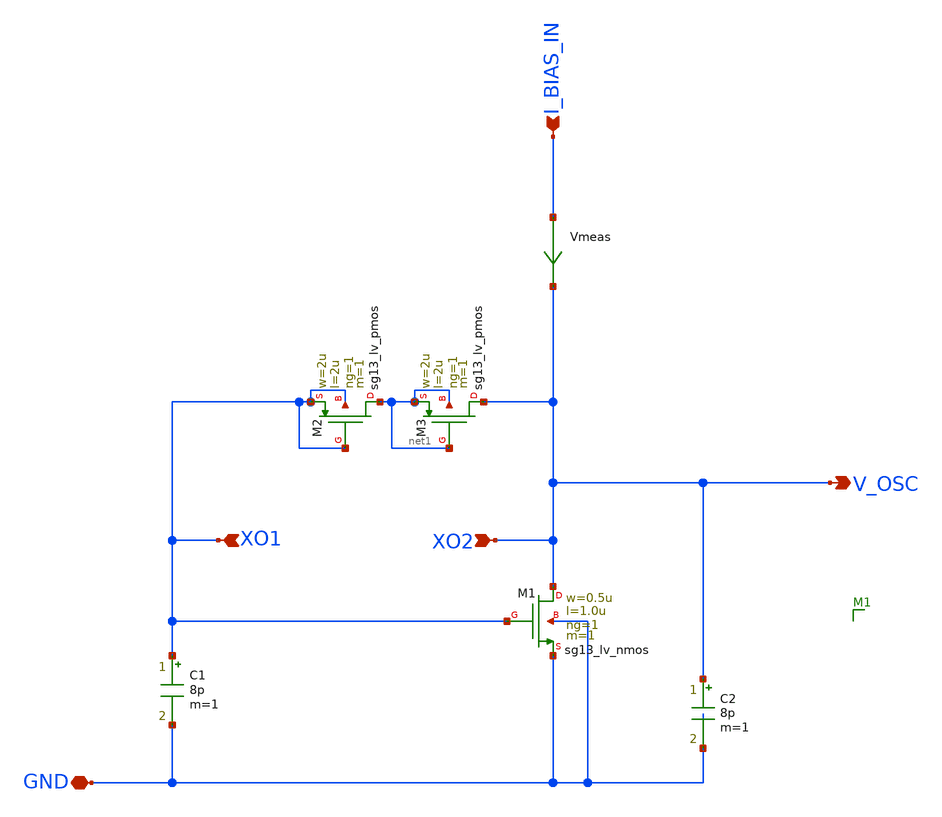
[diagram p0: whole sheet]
** sch_path: xo_core.sch
**.subckt xo_core GND XO2 XO1 I_BIAS_IN V_OSC
*.iopin GND
*.ipin XO2
*.ipin XO1
*.ipin I_BIAS_IN
*.opin V_OSC
XM2 net1 XO1 XO1 XO1 sg13_lv_pmos w=2u l=2u ng=1 m=1 mm_ok=1
XM3 XO2 net1 net1 net1 sg13_lv_pmos w=2u l=2u ng=1 m=1 mm_ok=1
XM1 XO2 XO1 GND GND sg13_lv_nmos w=0.5u l=1.0u ng=1 m=1 mm_ok=1
C2 XO2 GND 8p m=1
C1 XO1 GND 8p m=1
Vmeas I_BIAS_IN XO2 0
.save i(vmeas)
**.ends
.end
